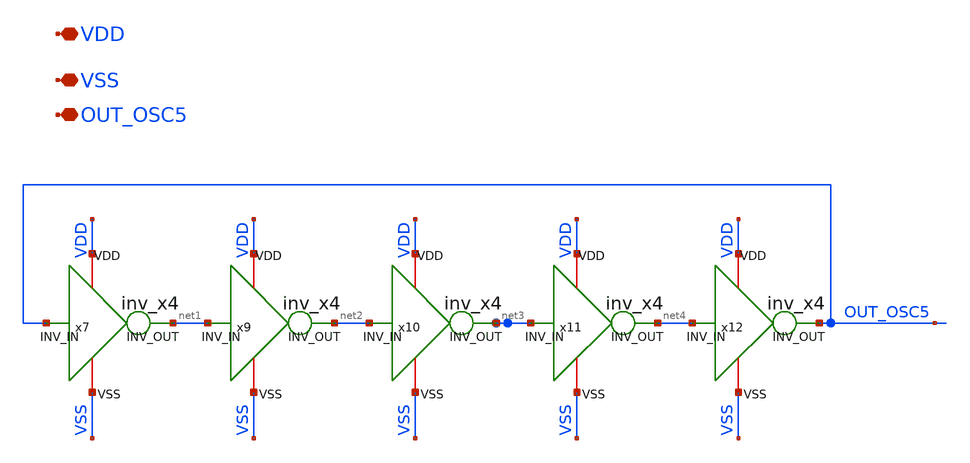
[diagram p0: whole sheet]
** sch_path: xschem/untitled-4.sch
**.subckt untitled-4 VDD VSS OUT_OSC5
*.iopin VDD
*.iopin VSS
*.iopin OUT_OSC5
x7 VDD VSS net1 OUT_OSC5 inv_x4
x9 VDD VSS net2 net1 inv_x4
x10 VDD VSS net3 net2 inv_x4
x11 VDD VSS net4 net3 inv_x4
x12 VDD VSS OUT_OSC5 net4 inv_x4
**.ends

* expanding   symbol:  inv_x4.sym # of pins=4
** sym_path: xschem/inv_x4.sym
** sch_path: xschem/inv_x4.sch
.subckt inv_x4 VDD VSS INV_OUT INV_IN
*.ipin INV_IN
*.opin INV_OUT
*.iopin VDD
*.iopin VSS
XM3 INV_OUT INV_IN VDD VDD sky130_fd_pr__pfet_01v8 L=10 W=2 nf=1 ad='int((nf+1)/2) * W/nf * 0.29' as='int((nf+2)/2) * W/nf * 0.29'
+ pd='2*int((nf+1)/2) * (W/nf + 0.29)' ps='2*int((nf+2)/2) * (W/nf + 0.29)' nrd='0.29 / W' nrs='0.29 / W'
+ sa=0 sb=0 sd=0 mult=1 m=1
XM5 INV_OUT INV_IN VSS VSS sky130_fd_pr__nfet_01v8 L=10 W=1 nf=1 ad='int((nf+1)/2) * W/nf * 0.29' as='int((nf+2)/2) * W/nf * 0.29'
+ pd='2*int((nf+1)/2) * (W/nf + 0.29)' ps='2*int((nf+2)/2) * (W/nf + 0.29)' nrd='0.29 / W' nrs='0.29 / W'
+ sa=0 sb=0 sd=0 mult=1 m=1
.ends

.end
